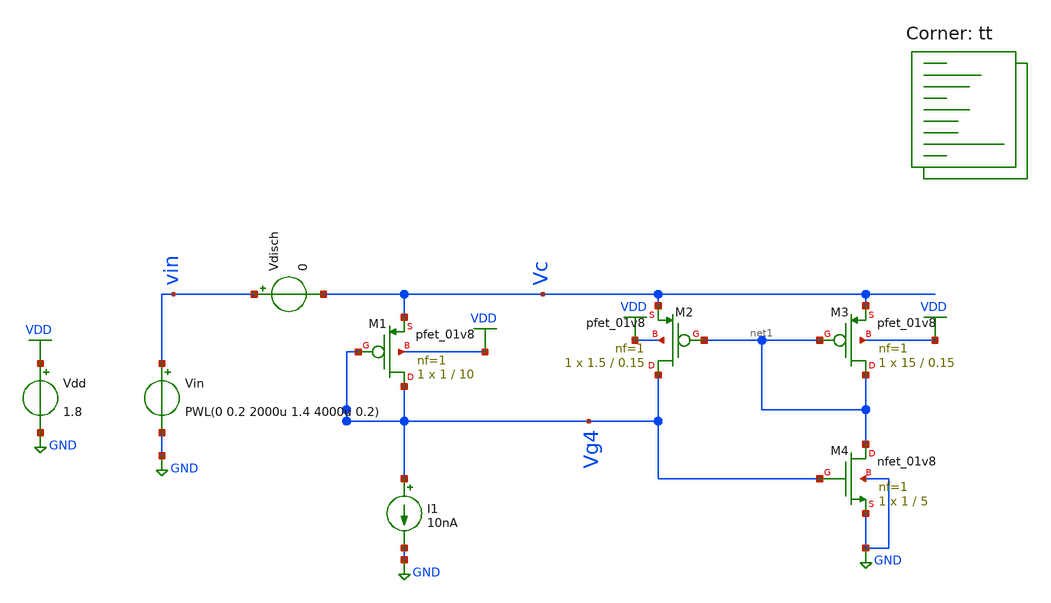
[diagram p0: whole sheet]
** sch_path: Neuron/ultralif/hysteresis_test.sch
**.subckt hysteresis_test
XM1 Vg4 Vg4 Vc VDD sky130_fd_pr__pfet_01v8 L=10 W=1 nf=1 ad='int((nf+1)/2) * W/nf * 0.29' as='int((nf+2)/2) * W/nf * 0.29'
+ pd='2*int((nf+1)/2) * (W/nf + 0.29)' ps='2*int((nf+2)/2) * (W/nf + 0.29)' nrd='0.29 / W' nrs='0.29 / W'
+ sa=0 sb=0 sd=0 mult=1 m=1
XM2 Vg4 net1 Vc VDD sky130_fd_pr__pfet_01v8 L=0.15 W=1.5 nf=1 ad='int((nf+1)/2) * W/nf * 0.29' as='int((nf+2)/2) * W/nf * 0.29'
+ pd='2*int((nf+1)/2) * (W/nf + 0.29)' ps='2*int((nf+2)/2) * (W/nf + 0.29)' nrd='0.29 / W' nrs='0.29 / W'
+ sa=0 sb=0 sd=0 mult=1 m=1
XM3 net1 net1 Vc VDD sky130_fd_pr__pfet_01v8 L=0.15 W=15 nf=1 ad='int((nf+1)/2) * W/nf * 0.29' as='int((nf+2)/2) * W/nf * 0.29'
+ pd='2*int((nf+1)/2) * (W/nf + 0.29)' ps='2*int((nf+2)/2) * (W/nf + 0.29)' nrd='0.29 / W' nrs='0.29 / W'
+ sa=0 sb=0 sd=0 mult=1 m=1
XM4 net1 Vg4 GND GND sky130_fd_pr__nfet_01v8 L=5 W=1 nf=1 ad='int((1 + 1)/2) * 1 / 1 * 0.29' as='int((1 + 2)/2) * 1 / 1 * 0.29'
+ pd='2*int((1 + 1)/2) * (1 / 1 + 0.29)' ps='2*int((1 + 2)/2) * (1 / 1 + 0.29)' nrd='0.29 / 1 ' nrs='0.29 / 1 '
+ sa=0 sb=0 sd=0 mult=1 m=1
I1 Vg4 GND 10nA
Vin vin GND PWL(0 0.2 2000u 1.4 4000u 0.2)
Vdisch vin Vc 0
Vdd VDD GND 1.8
**** begin user architecture code
.lib $::SKYWATER_MODELS/sky130.lib.spice tt
**** end user architecture code
**.ends
.GLOBAL GND
.GLOBAL VDD
**** begin user architecture code

.options savecurrents
.tran 100n 4000u
*.dc Vin 0.2 0.7 0.01
.save all
.control
	run
	write hysteresis_test.raw
*plot all.Vout
.endc


**** end user architecture code
.end
